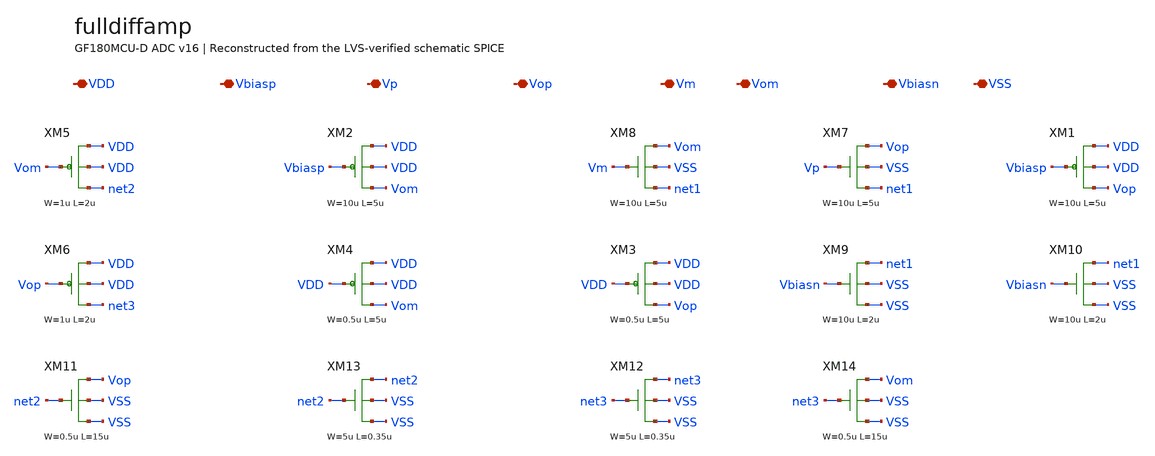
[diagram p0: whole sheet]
** sch_path: src/schematics/INTEGRATION/ADC_final/ADC_v17_Xschem/fulldiffamp.sch
* Copyright (C) 1998-2026 Stefan Frederik Schippers
* This program is free software; you can redistribute it and/or modify
* it under the terms of the GNU General Public License as published by
* the Free Software Foundation; either version 2 of the License, or
* (at your option) any later version.
**.subckt fulldiffamp VDD Vbiasp Vp Vop Vm Vom Vbiasn VSS
*.iopin VDD
*.iopin Vbiasp
*.iopin Vp
*.iopin Vop
*.iopin Vm
*.iopin Vom
*.iopin Vbiasn
*.iopin VSS
XM5 net2 Vom VDD VDD pfet_03v3 L=2u W=1u nf=1 ad='int((nf+1)/2) * W/nf * 0.18u' as='int((nf+2)/2) * W/nf * 0.18u'
+ pd='2*int((nf+1)/2) * (W/nf + 0.18u)' ps='2*int((nf+2)/2) * (W/nf + 0.18u)' nrd='0.18u / W' nrs='0.18u / W'
+ sa=0 sb=0 sd=0
XM2 Vom Vbiasp VDD VDD pfet_03v3 L=5u W=10u nf=1 ad='int((nf+1)/2) * W/nf * 0.18u' as='int((nf+2)/2) * W/nf * 0.18u'
+ pd='2*int((nf+1)/2) * (W/nf + 0.18u)' ps='2*int((nf+2)/2) * (W/nf + 0.18u)' nrd='0.18u / W' nrs='0.18u / W'
+ sa=0 sb=0 sd=0
XM8 Vom Vm net1 VSS nfet_03v3 L=5u W=10u nf=1 ad='int((nf+1)/2) * W/nf * 0.18u' as='int((nf+2)/2) * W/nf * 0.18u'
+ pd='2*int((nf+1)/2) * (W/nf + 0.18u)' ps='2*int((nf+2)/2) * (W/nf + 0.18u)' nrd='0.18u / W' nrs='0.18u / W'
+ sa=0 sb=0 sd=0
XM7 Vop Vp net1 VSS nfet_03v3 L=5u W=10u nf=1 ad='int((nf+1)/2) * W/nf * 0.18u' as='int((nf+2)/2) * W/nf * 0.18u'
+ pd='2*int((nf+1)/2) * (W/nf + 0.18u)' ps='2*int((nf+2)/2) * (W/nf + 0.18u)' nrd='0.18u / W' nrs='0.18u / W'
+ sa=0 sb=0 sd=0
XM1 Vop Vbiasp VDD VDD pfet_03v3 L=5u W=10u nf=1 ad='int((nf+1)/2) * W/nf * 0.18u' as='int((nf+2)/2) * W/nf * 0.18u'
+ pd='2*int((nf+1)/2) * (W/nf + 0.18u)' ps='2*int((nf+2)/2) * (W/nf + 0.18u)' nrd='0.18u / W' nrs='0.18u / W'
+ sa=0 sb=0 sd=0
XM6 net3 Vop VDD VDD pfet_03v3 L=2u W=1u nf=1 ad='int((nf+1)/2) * W/nf * 0.18u' as='int((nf+2)/2) * W/nf * 0.18u'
+ pd='2*int((nf+1)/2) * (W/nf + 0.18u)' ps='2*int((nf+2)/2) * (W/nf + 0.18u)' nrd='0.18u / W' nrs='0.18u / W'
+ sa=0 sb=0 sd=0
XM4 Vom VDD VDD VDD pfet_03v3 L=5u W=0.5u nf=1 ad='int((nf+1)/2) * W/nf * 0.18u' as='int((nf+2)/2) * W/nf * 0.18u'
+ pd='2*int((nf+1)/2) * (W/nf + 0.18u)' ps='2*int((nf+2)/2) * (W/nf + 0.18u)' nrd='0.18u / W' nrs='0.18u / W'
+ sa=0 sb=0 sd=0
XM3 Vop VDD VDD VDD pfet_03v3 L=5u W=0.5u nf=1 ad='int((nf+1)/2) * W/nf * 0.18u' as='int((nf+2)/2) * W/nf * 0.18u'
+ pd='2*int((nf+1)/2) * (W/nf + 0.18u)' ps='2*int((nf+2)/2) * (W/nf + 0.18u)' nrd='0.18u / W' nrs='0.18u / W'
+ sa=0 sb=0 sd=0
XM9 net1 Vbiasn VSS VSS nfet_03v3 L=2u W=10u nf=1 ad='int((nf+1)/2) * W/nf * 0.18u' as='int((nf+2)/2) * W/nf * 0.18u'
+ pd='2*int((nf+1)/2) * (W/nf + 0.18u)' ps='2*int((nf+2)/2) * (W/nf + 0.18u)' nrd='0.18u / W' nrs='0.18u / W'
+ sa=0 sb=0 sd=0
XM10 net1 Vbiasn VSS VSS nfet_03v3 L=2u W=10u nf=1 ad='int((nf+1)/2) * W/nf * 0.18u' as='int((nf+2)/2) * W/nf * 0.18u'
+ pd='2*int((nf+1)/2) * (W/nf + 0.18u)' ps='2*int((nf+2)/2) * (W/nf + 0.18u)' nrd='0.18u / W' nrs='0.18u / W'
+ sa=0 sb=0 sd=0
XM11 Vop net2 VSS VSS nfet_03v3 L=15u W=0.5u nf=1 ad='int((nf+1)/2) * W/nf * 0.18u' as='int((nf+2)/2) * W/nf * 0.18u'
+ pd='2*int((nf+1)/2) * (W/nf + 0.18u)' ps='2*int((nf+2)/2) * (W/nf + 0.18u)' nrd='0.18u / W' nrs='0.18u / W'
+ sa=0 sb=0 sd=0
XM13 net2 net2 VSS VSS nfet_03v3 L=0.35u W=5u nf=1 ad='int((nf+1)/2) * W/nf * 0.18u' as='int((nf+2)/2) * W/nf * 0.18u'
+ pd='2*int((nf+1)/2) * (W/nf + 0.18u)' ps='2*int((nf+2)/2) * (W/nf + 0.18u)' nrd='0.18u / W' nrs='0.18u / W'
+ sa=0 sb=0 sd=0
XM12 net3 net3 VSS VSS nfet_03v3 L=0.35u W=5u nf=1 ad='int((nf+1)/2) * W/nf * 0.18u' as='int((nf+2)/2) * W/nf * 0.18u'
+ pd='2*int((nf+1)/2) * (W/nf + 0.18u)' ps='2*int((nf+2)/2) * (W/nf + 0.18u)' nrd='0.18u / W' nrs='0.18u / W'
+ sa=0 sb=0 sd=0
XM14 Vom net3 VSS VSS nfet_03v3 L=15u W=0.5u nf=1 ad='int((nf+1)/2) * W/nf * 0.18u' as='int((nf+2)/2) * W/nf * 0.18u'
+ pd='2*int((nf+1)/2) * (W/nf + 0.18u)' ps='2*int((nf+2)/2) * (W/nf + 0.18u)' nrd='0.18u / W' nrs='0.18u / W'
+ sa=0 sb=0 sd=0
**.ends
.end
